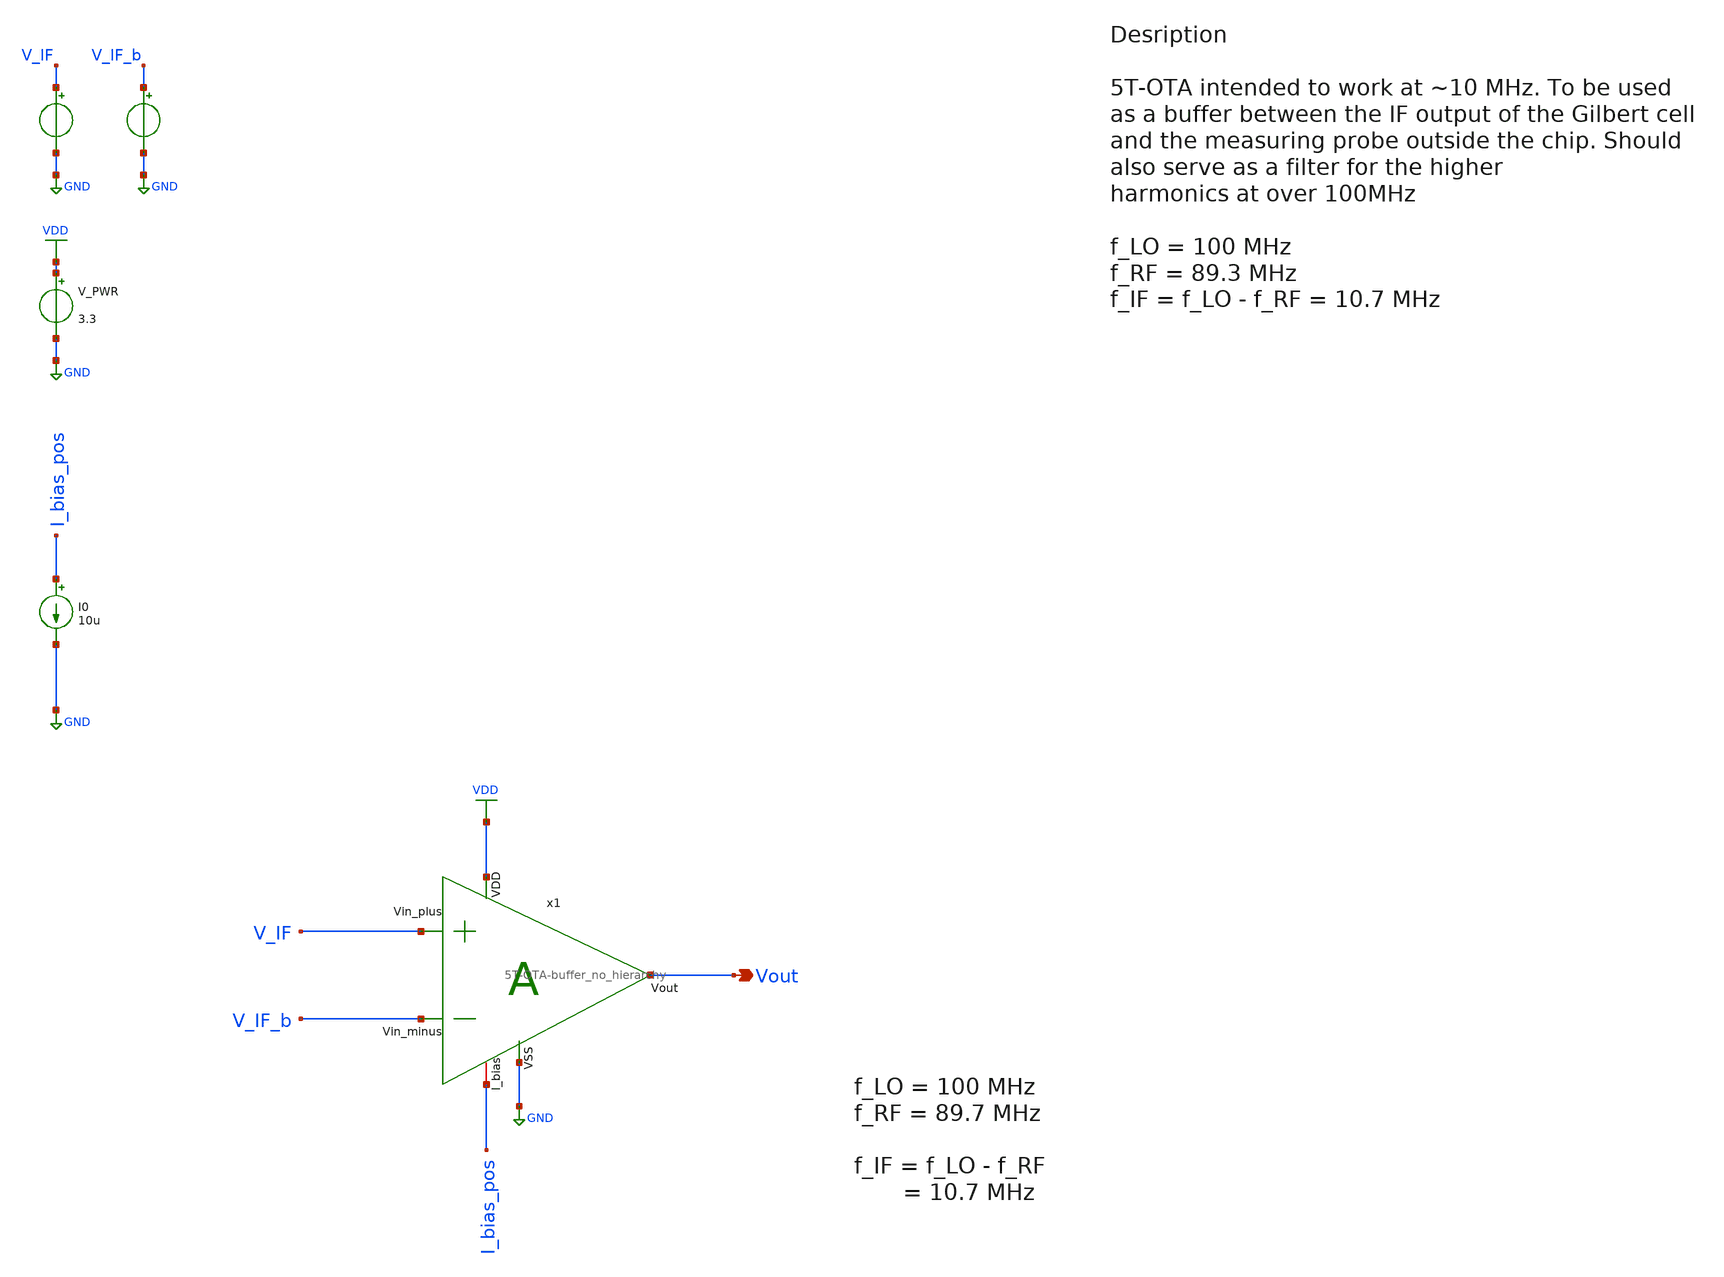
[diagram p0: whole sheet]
** sch_path: src/design_tb/5T-OTA_tb.sch
**.subckt 5T-OTA_tb Vout
*.opin Vout
V_PWR VDD GND 3.3
.save i(v_pwr)
V_IF V_IF GND sin( 1 1 1 0 )
.save i(v_if)
V_IF_b V_IF_b GND sin( 1 1 1 0 )
.save i(v_if_b)
I0 I_bias_pos GND 10u
x1 VDD Vout V_IF V_IF_b I_bias_pos GND 5T-OTA-buffer_no_hierarchy
**** begin user architecture code

.include $::180MCU_MODELS/design.ngspice
.lib $::180MCU_MODELS/sm141064.ngspice typical
.lib $::180MCU_MODELS/sm141064.ngspice mimcap_typical
.lib $::180MCU_MODELS/sm141064.ngspice cap_mim
.lib $::180MCU_MODELS/sm141064.ngspice res_typical




* let sets vectors to a plot, while set sets a variable, globally accessible in .control
.control

    * Set frequency and amplitude variables to proper values from within the control sequence
    * sine-wave L

    set freq_if = 10.7Meg
    set cm_if = 2
    set amp_if = 0.5

    * set the parameters to the voltage sources
    alter @V_IF[sin] = [ $cm_if $amp_if $freq_if 0 ]
    alter @V_IF_b[sin] = [ $cm_if $amp_if $freq_if 0 0 180 ]

    save all

    * operating point
    op
    show
    write 5T-OTA.raw

    set appendwrite

    * Transient analysis to observe mixing operation
    tran 3p 300n
    write 5T-OTA.raw


.endc


**** end user architecture code
**.ends

* expanding   symbol:
*+  /home/vasil/Downloads/SSCS_PICO_2025/src/design_xsch/5T-OTA-buffer_no_hierarchy.sym # of pins=6
** sym_path: src/design_xsch/5T-OTA-buffer_no_hierarchy.sym
** sch_path: src/design_xsch/5T-OTA-buffer_no_hierarchy.sch
.subckt 5T-OTA-buffer_no_hierarchy VDD Vout Vin_plus Vin_minus I_bias VSS
*.ipin VDD
*.ipin Vin_plus
*.ipin Vin_minus
*.opin Vout
*.iopin I_bias
*.ipin VSS
XM3 net1 Vin_plus I_bias VSS nfet_03v3 L=0.28u W=7u nf=4 ad='int((nf+1)/2) * W/nf * 0.18u' as='int((nf+2)/2) * W/nf * 0.18u'
+ pd='2*int((nf+1)/2) * (W/nf + 0.18u)' ps='2*int((nf+2)/2) * (W/nf + 0.18u)' nrd='0.18u / W' nrs='0.18u / W'
+ sa=0 sb=0 sd=0 m=1
XM4 Vout Vin_minus I_bias VSS nfet_03v3 L=0.28u W=7u nf=4 ad='int((nf+1)/2) * W/nf * 0.18u' as='int((nf+2)/2) * W/nf * 0.18u'
+ pd='2*int((nf+1)/2) * (W/nf + 0.18u)' ps='2*int((nf+2)/2) * (W/nf + 0.18u)' nrd='0.18u / W' nrs='0.18u / W'
+ sa=0 sb=0 sd=0 m=1
XM1 net1 net1 VDD VDD pfet_03v3 L=0.28u W=17u nf=5 ad='int((nf+1)/2) * W/nf * 0.18u' as='int((nf+2)/2) * W/nf * 0.18u'
+ pd='2*int((nf+1)/2) * (W/nf + 0.18u)' ps='2*int((nf+2)/2) * (W/nf + 0.18u)' nrd='0.18u / W' nrs='0.18u / W'
+ sa=0 sb=0 sd=0 m=1
XM2 Vout net1 VDD VDD pfet_03v3 L=0.28u W=17u nf=5 ad='int((nf+1)/2) * W/nf * 0.18u' as='int((nf+2)/2) * W/nf * 0.18u'
+ pd='2*int((nf+1)/2) * (W/nf + 0.18u)' ps='2*int((nf+2)/2) * (W/nf + 0.18u)' nrd='0.18u / W' nrs='0.18u / W'
+ sa=0 sb=0 sd=0 m=1
.ends

.GLOBAL VDD
.GLOBAL GND
.end
